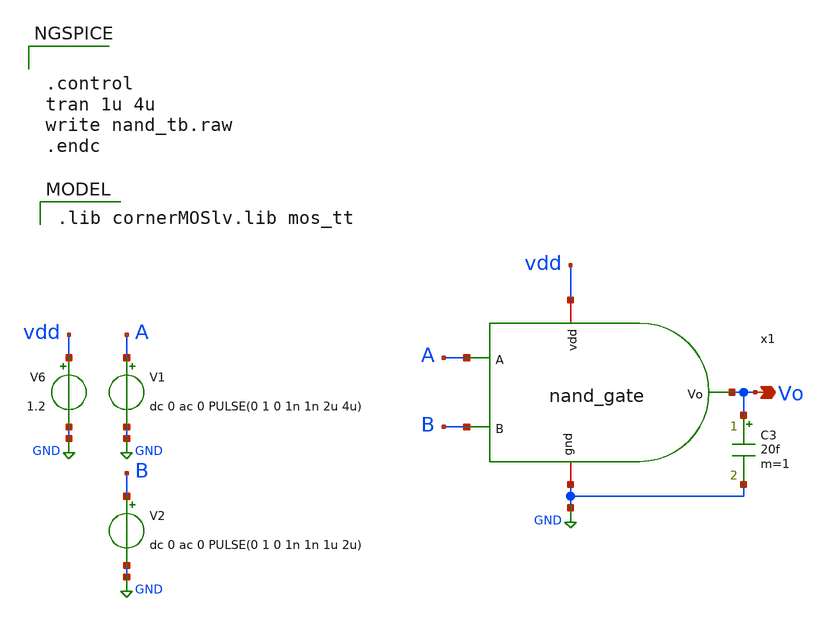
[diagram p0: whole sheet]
** sch_path: dependencies/ADC/dependencies/SAR_ADC_8BIT_IHP/xschem/nand_tb.sch
**.subckt nand_tb Vo
*.opin Vo
V1 A GND dc 0 ac 0 PULSE(0 1 0 1n 1n 2u 4u)
V6 vdd GND 1.2
V2 B GND dc 0 ac 0 PULSE(0 1 0 1n 1n 1u 2u)
x1 vdd Vo B A GND nand_gate
C3 Vo GND 20f m=1
**** begin user architecture code


.control
tran 1u 4u
write nand_tb.raw
.endc


 .lib cornerMOSlv.lib mos_tt

**** end user architecture code
**.ends
.GLOBAL GND
.end
